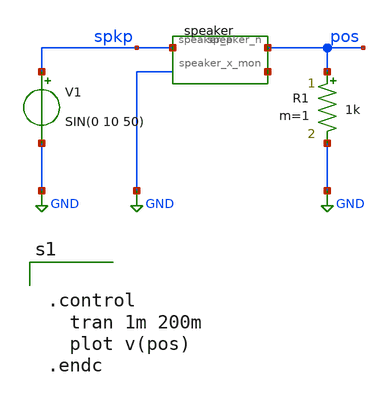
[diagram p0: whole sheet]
** sch_path: examples/analog_speaker/tran.sch
**.subckt tran
Xspeaker1 spkp pos net1 speaker
R1 pos GND 1k m=1
V1 spkp GND SIN(0 10 50)
**** begin user architecture code


.control
  tran 1m 200m
  plot v(pos)
.endc


**** end user architecture code
**.ends

* expanding   symbol:  speaker.sym # of pins=3
** sym_path: examples/analog_speaker/speaker.sym
.include /workspace/speaker.spice
.GLOBAL GND
.end
